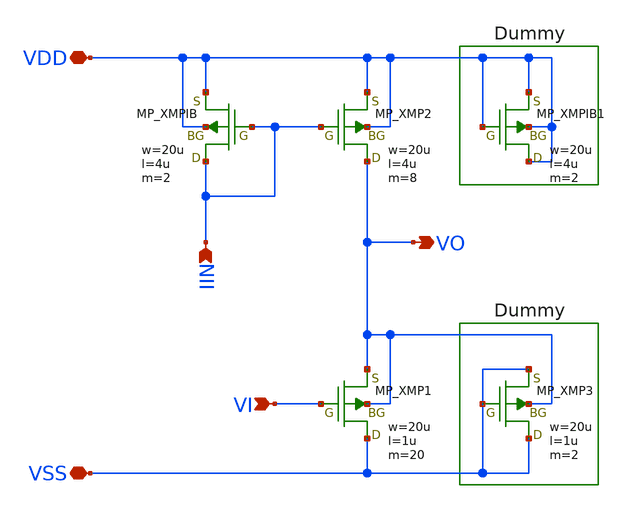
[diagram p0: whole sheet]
** sch_path: member_project/BGR/Maehashi/design/psf.sch
**.subckt psf IIN VSS VDD VO VI
*.ipin IIN
*.iopin VSS
*.iopin VDD
*.opin VO
*.ipin VI
XXMPIB IIN IIN VDD VDD PMOS w=20u l=4u as=0 ad=0 ps=0 pd=0 nrd=0 nrs=0 m=2
XXMP2 VO IIN VDD VDD PMOS w=20u l=4u as=0 ad=0 ps=0 pd=0 nrd=0 nrs=0 m=8
XXMP1 VSS VI VO VO PMOS w=20u l=1u as=0 ad=0 ps=0 pd=0 nrd=0 nrs=0 m=20
XXMP3 VSS VSS VSS VO PMOS w=20u l=1u as=0 ad=0 ps=0 pd=0 nrd=0 nrs=0 m=2
XXMPIB1 VDD VDD VDD VDD PMOS w=20u l=4u as=0 ad=0 ps=0 pd=0 nrd=0 nrs=0 m=2
**.ends
.end
